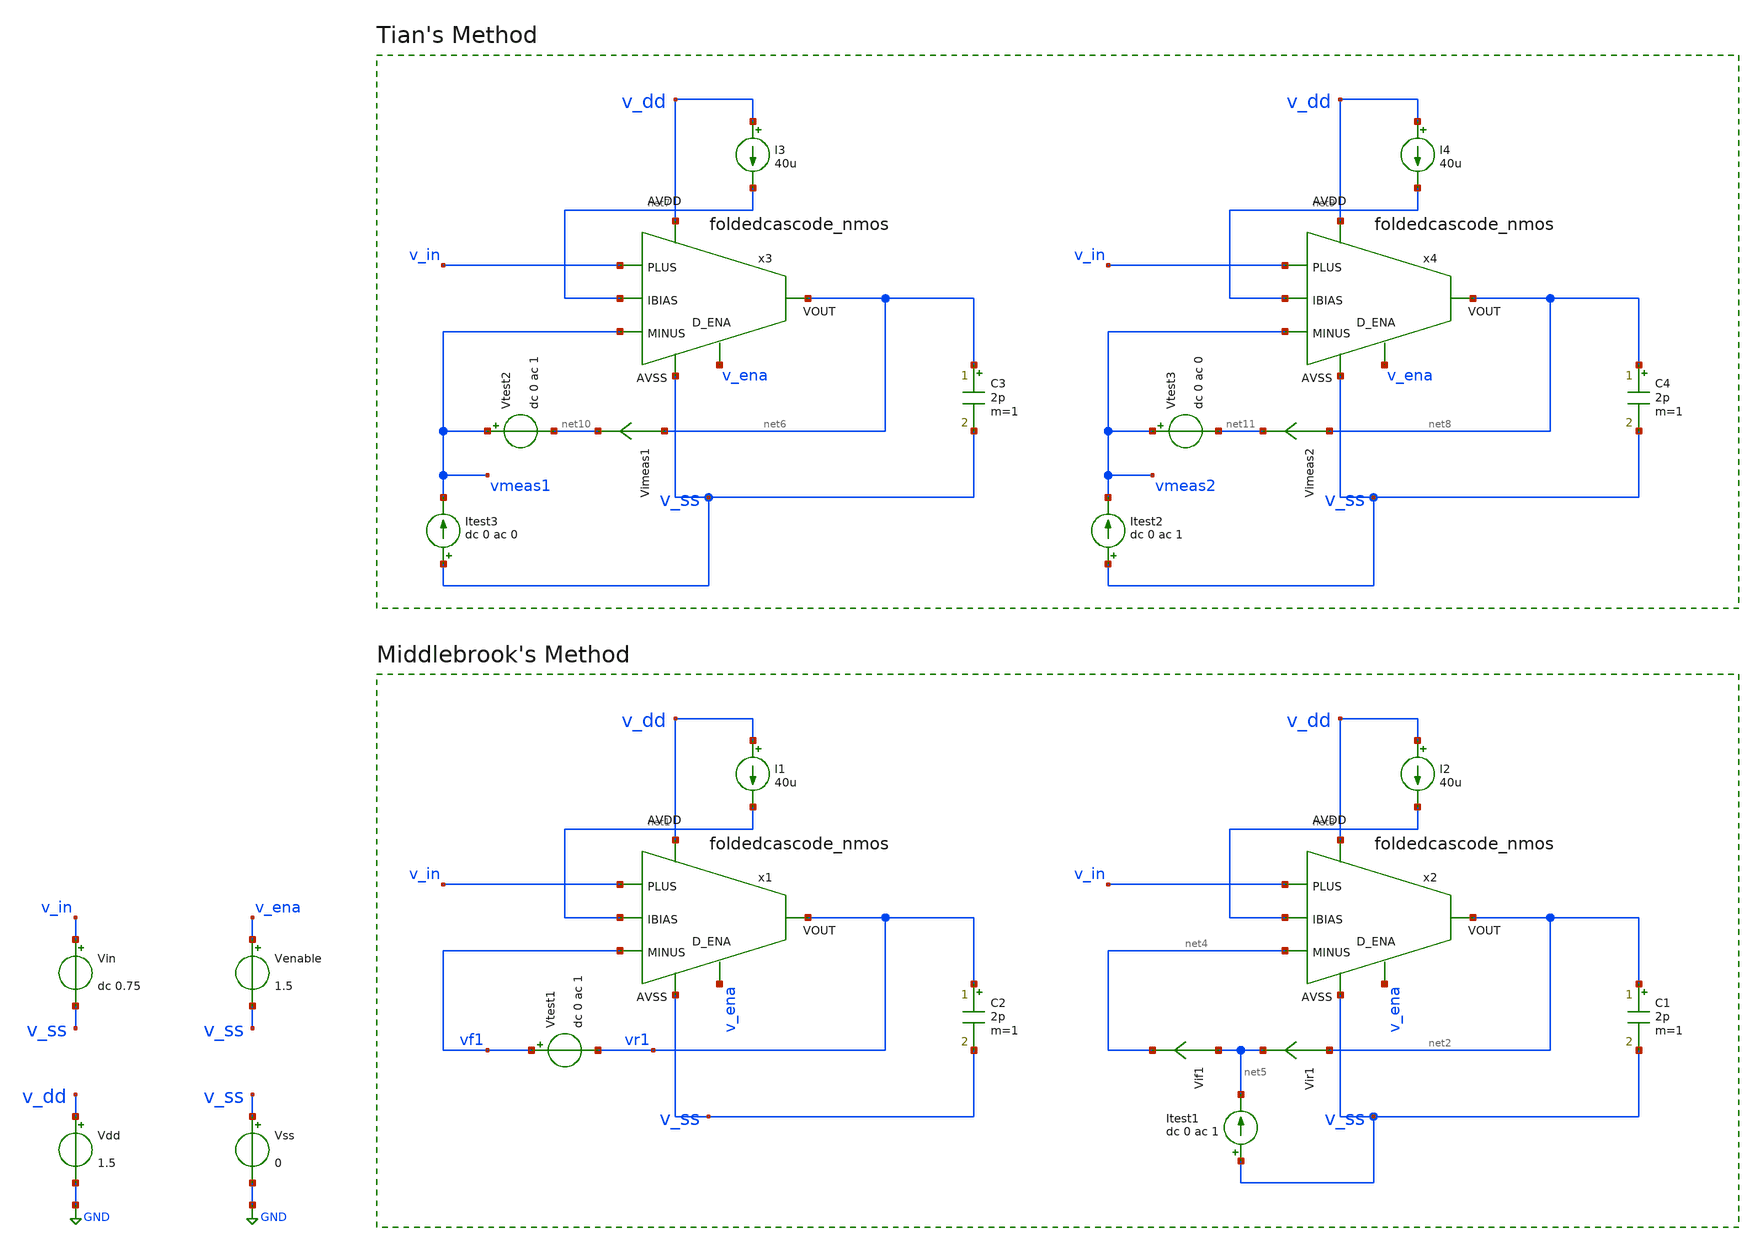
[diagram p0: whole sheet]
** sch_path: DSM_2ndOrder/1_Schematics/real_circuits/1v2/tb_foldedcascode_nmos_loopgain.sch
* (c) 2025 Thesis_HP, Apache-2.0 license
**.subckt tb_foldedcascode_nmos_loopgain
Vdd v_dd GND 1.5
Vss v_ss GND 0
Vin v_in v_ss dc 0.75
C2 vr1 v_ss 2p m=1
I1 v_dd net1 40u
Vtest1 vf1 vr1 dc 0 ac 1
C1 net2 v_ss 2p m=1
I2 v_dd net3 40u
Vir1 net2 net5 0
.save i(vir1)
Vif1 net5 net4 0
.save i(vif1)
Itest1 v_ss net5 dc 0 ac 1
C3 net6 v_ss 2p m=1
I3 v_dd net7 40u
C4 net8 v_ss 2p m=1
I4 v_dd net9 40u
Itest3 v_ss vmeas1 dc 0 ac 0
Vtest2 vmeas1 net10 dc 0 ac 1
Vimeas1 net6 net10 0
.save i(vimeas1)
Itest2 v_ss vmeas2 dc 0 ac 1
Vtest3 vmeas2 net11 dc 0 ac 0
Vimeas2 net8 net11 0
.save i(vimeas2)
x3 v_dd net7 net6 vmeas1 v_in v_ena v_ss foldedcascode_nmos
x4 v_dd net9 net8 vmeas2 v_in v_ena v_ss foldedcascode_nmos
x1 v_dd net1 vr1 vf1 v_in v_ena v_ss foldedcascode_nmos
x2 v_dd net3 net2 net4 v_in v_ena v_ss foldedcascode_nmos
Venable v_ena v_ss 1.5
**** begin user architecture code

.lib cornerMOSlv.lib mos_tt
.lib cornerRES.lib res_typ




*.include /foss/designs/thesis/thesis_hp/designs/otas/3_kpex/foldedcascode_nmos_withdummies__foldedcascode_nmos_withdummies/magic_CC/foldedcascode_nmos_withdummies.pex.spice


.param temp=27
.options savecurrents reltol=1e-3 abstol=1e-12 gmin=1e-15
.control
save all

* Operating Point Analysis
op

* AC Analysis
ac dec 101 1 100G
remzerovec

* Middlebrook's Method
let tv  = -v(vr1)/v(vf1)
let ti  = -i(vir1)/i(vif1)
let tmb = (tv*ti - 1)/(tv + ti + 2)

* Tian's Method
* vtest=0, itest=1:
let A = i(Vimeas2)
let C = v(vmeas2)

* vtest=1, itest=0:
let B = i(Vimeas1)
let D = v(vmeas1)
let ttian = (A*D - B*C - A)/(2*(B*C - A*D) + A - D + 1)

optional interactive plots
plot db(tmb) ylabel 'Magnitude - Middlebrook'
plot 180/pi*cphase(tmb) ylabel 'Phase - Middlebrook'
plot db(ttian) ylabel 'Magnitude - Tian'
plot 180/pi*cphase(ttian) ylabel 'Phase - Tian'
plot db(tmb) db(ttian) ylabel 'Magnitude'
plot 180/pi*cphase(tmb) 180/pi*cphase(ttian) ylabel 'Phase'

* SINGLE clean write at the end
write foldedcascode_nmos_tb-loopgain.raw

.endc


**** end user architecture code
**.ends
.GLOBAL GND
.end
